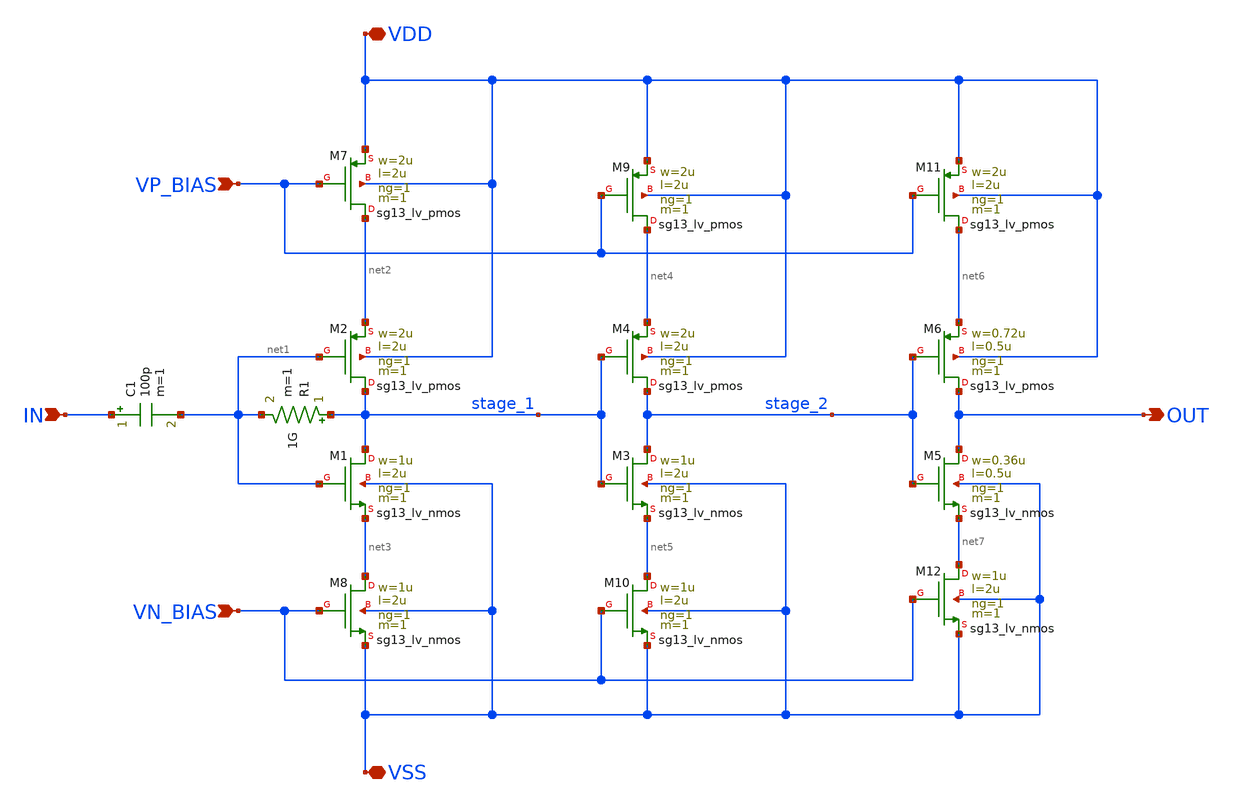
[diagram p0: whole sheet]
** sch_path: clock_gen.sch
**.subckt clock_gen VSS VDD IN OUT VP_BIAS VN_BIAS
*.iopin VSS
*.iopin VDD
*.ipin IN
*.opin OUT
*.ipin VP_BIAS
*.ipin VN_BIAS
XM1 stage_1 net1 net3 VSS sg13_lv_nmos w=1u l=2u ng=1 m=1 mm_ok=1
XM2 stage_1 net1 net2 VDD sg13_lv_pmos w=2u l=2u ng=1 m=1 mm_ok=1
R1 stage_1 net1 1G m=1
C1 IN net1 100p m=1
XM3 stage_2 stage_1 net5 VSS sg13_lv_nmos w=1u l=2u ng=1 m=1 mm_ok=1
XM4 stage_2 stage_1 net4 VDD sg13_lv_pmos w=2u l=2u ng=1 m=1 mm_ok=1
XM5 OUT stage_2 net7 VSS sg13_lv_nmos w=0.36u l=0.5u ng=1 m=1 mm_ok=1
XM6 OUT stage_2 net6 VDD sg13_lv_pmos w=0.72u l=0.5u ng=1 m=1 mm_ok=1
XM7 net2 VP_BIAS VDD VDD sg13_lv_pmos w=2u l=2u ng=1 m=1 mm_ok=1
XM8 net3 VN_BIAS VSS VSS sg13_lv_nmos w=1u l=2u ng=1 m=1 mm_ok=1
XM9 net4 VP_BIAS VDD VDD sg13_lv_pmos w=2u l=2u ng=1 m=1 mm_ok=1
XM10 net5 VN_BIAS VSS VSS sg13_lv_nmos w=1u l=2u ng=1 m=1 mm_ok=1
XM11 net6 VP_BIAS VDD VDD sg13_lv_pmos w=2u l=2u ng=1 m=1 mm_ok=1
XM12 net7 VN_BIAS VSS VSS sg13_lv_nmos w=1u l=2u ng=1 m=1 mm_ok=1
**.ends
.end
